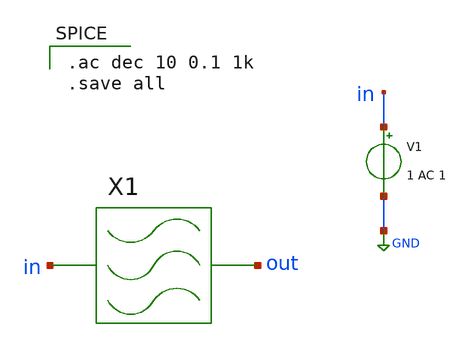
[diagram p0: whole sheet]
** sch_path: xschem/FILTER/ideal_FILTER_TB.sch
**.subckt ideal_FILTER_TB
X1 in out ideal_FILTER
V1 in GND 1 AC 1
**** begin user architecture code

.ac dec 10 0.1 1k
.save all

**** end user architecture code
**.ends

* expanding   symbol:  FILTER/ideal_FILTER.sym # of pins=2
** sym_path: xschem/FILTER/ideal_FILTER.sym
** sch_path: xschem/FILTER/ideal_FILTER.sch
.subckt ideal_FILTER vin vout
*.ipin vin
*.opin vout
X1 vin net1 net1 opamp
X2 net3 net2 net2 opamp
X3 net4 vout vout opamp
R1 net3 net1 1k m=1
R2 net4 GND 10k m=1
C1 net3 GND 5.3u m=1
C2 net4 net2 1.6u m=1
.ends


* expanding   symbol:  MISC/opamp.sym # of pins=3
** sym_path: xschem/MISC/opamp.sym
** sch_path: xschem/MISC/opamp.sch
.subckt opamp vp vm out
*.ipin vp
*.ipin vm
*.opin out
E1 out GND vp vm 1E6
.ends

.GLOBAL GND
.end
